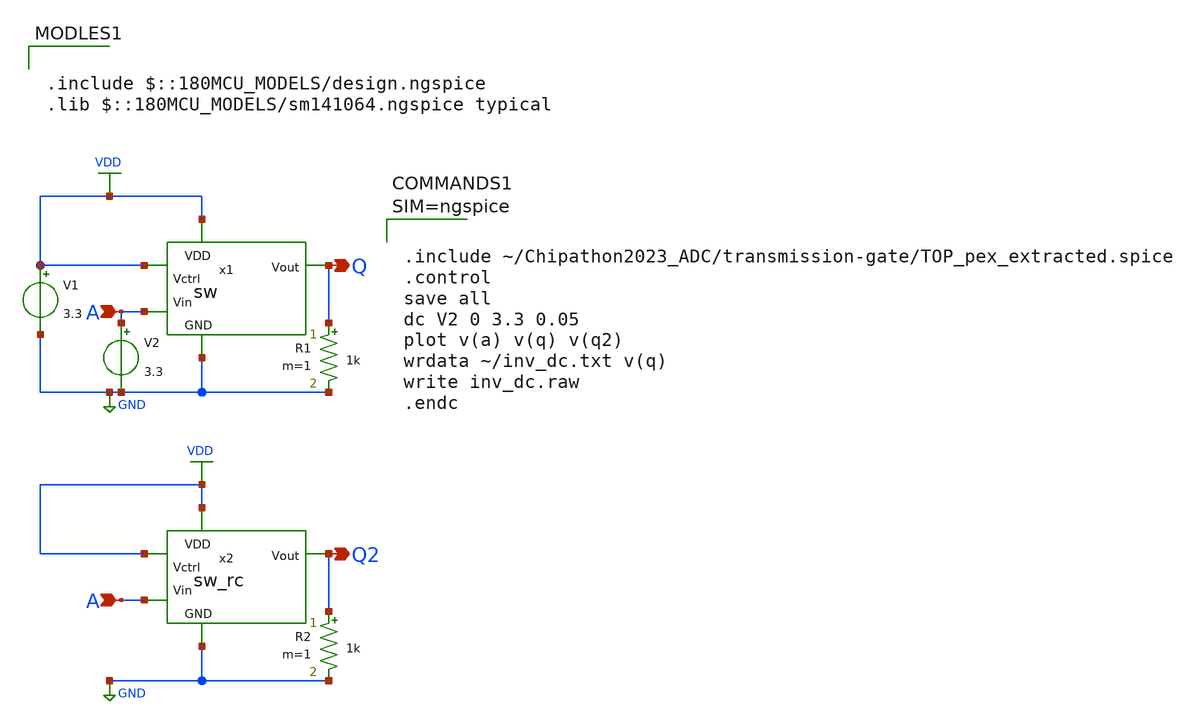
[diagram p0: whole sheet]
** sch_path: review/0407/transmission-gate/sw_test.sch
**.subckt sw_test A Q A Q2
*.ipin A
*.opin Q
*.ipin A
*.opin Q2
V1 VDD GND 3.3
V2 A GND 3.3
x1 VDD VDD Q A GND sw
R1 Q GND 1k m=1
R2 Q2 GND 1k m=1
x2 VDD GND Q2 A VDD TOP
**** begin user architecture code

.include $::180MCU_MODELS/design.ngspice
.lib $::180MCU_MODELS/sm141064.ngspice typical




.include ~/Chipathon2023_ADC/transmission-gate/TOP_pex_extracted.spice
.control
save all
dc V2 0 3.3 0.05
plot v(a) v(q) v(q2)
wrdata ~/inv_dc.txt v(q)
write inv_dc.raw
.endc



**** end user architecture code
**.ends

* expanding   symbol:  sw.sym # of pins=5
** sym_path: transmission-gate/sw.sym
** sch_path: transmission-gate/sw.sch
.subckt sw Vctrl VDD Vout Vin GND
*.ipin Vctrl
*.ipin Vin
*.opin Vout
*.ipin VDD
*.ipin GND
XM1 Vin net1 Vout VDD pfet_03v3 L=0.28u W=2.8u nf=1 ad='int((nf+1)/2) * W/nf * 0.18u' as='int((nf+2)/2) * W/nf * 0.18u'
+ pd='2*int((nf+1)/2) * (W/nf + 0.18u)' ps='2*int((nf+2)/2) * (W/nf + 0.18u)' nrd='0.18u / W' nrs='0.18u / W'
+ sa=0 sb=0 sd=0 m=1
XM2 Vin Vctrl Vout GND nfet_03v3 L=0.28u W=2.8u nf=1 ad='int((nf+1)/2) * W/nf * 0.18u' as='int((nf+2)/2) * W/nf * 0.18u'
+ pd='2*int((nf+1)/2) * (W/nf + 0.18u)' ps='2*int((nf+2)/2) * (W/nf + 0.18u)' nrd='0.18u / W' nrs='0.18u / W'
+ sa=0 sb=0 sd=0 m=1
XM3 net1 Vctrl VDD VDD pfet_03v3 L=0.28u W=2.8u nf=1 ad='int((nf+1)/2) * W/nf * 0.18u' as='int((nf+2)/2) * W/nf * 0.18u'
+ pd='2*int((nf+1)/2) * (W/nf + 0.18u)' ps='2*int((nf+2)/2) * (W/nf + 0.18u)' nrd='0.18u / W' nrs='0.18u / W'
+ sa=0 sb=0 sd=0 m=1
XM4 net1 Vctrl GND GND nfet_03v3 L=0.28u W=2.8u nf=1 ad='int((nf+1)/2) * W/nf * 0.18u' as='int((nf+2)/2) * W/nf * 0.18u'
+ pd='2*int((nf+1)/2) * (W/nf + 0.18u)' ps='2*int((nf+2)/2) * (W/nf + 0.18u)' nrd='0.18u / W' nrs='0.18u / W'
+ sa=0 sb=0 sd=0 m=1
.ends

.GLOBAL GND
.GLOBAL VDD
.end
